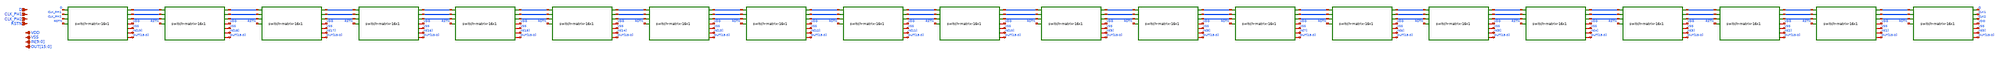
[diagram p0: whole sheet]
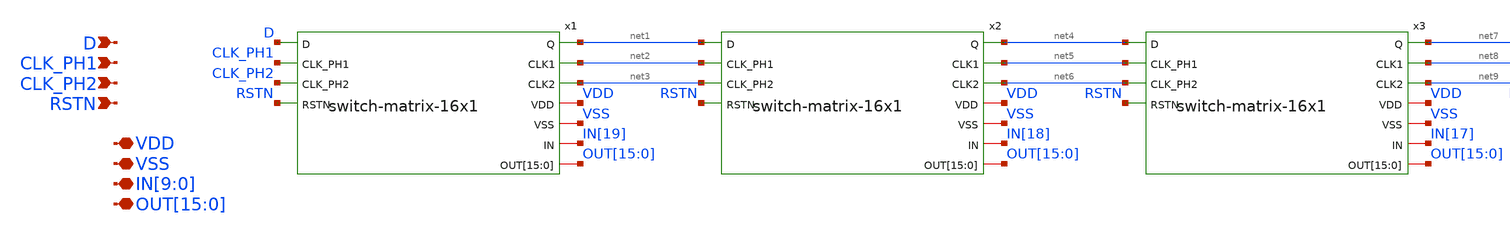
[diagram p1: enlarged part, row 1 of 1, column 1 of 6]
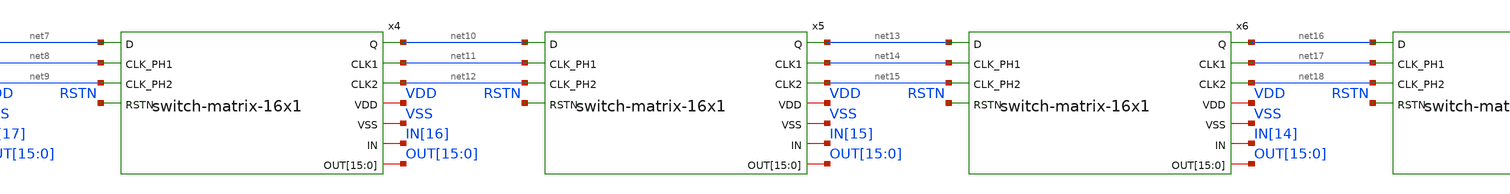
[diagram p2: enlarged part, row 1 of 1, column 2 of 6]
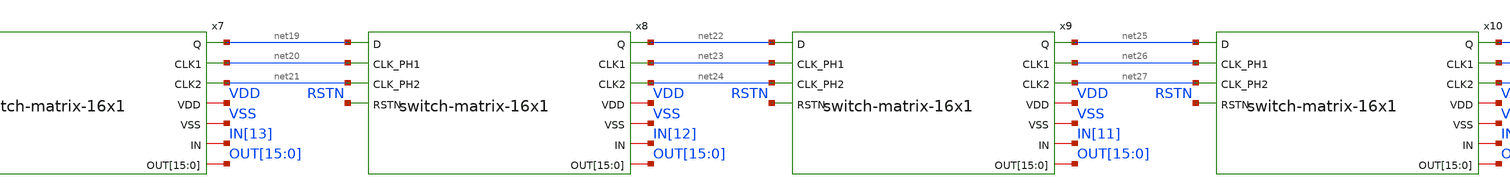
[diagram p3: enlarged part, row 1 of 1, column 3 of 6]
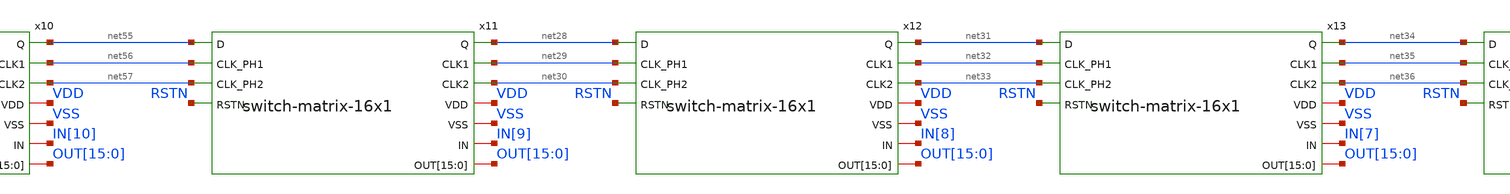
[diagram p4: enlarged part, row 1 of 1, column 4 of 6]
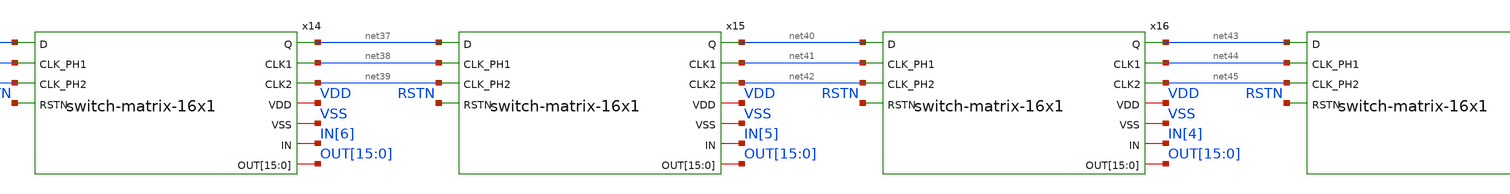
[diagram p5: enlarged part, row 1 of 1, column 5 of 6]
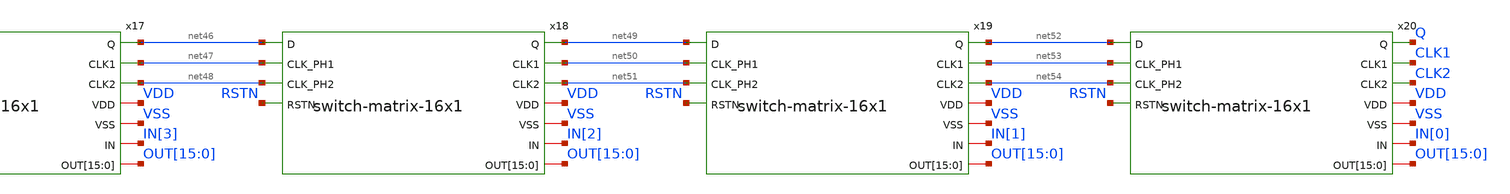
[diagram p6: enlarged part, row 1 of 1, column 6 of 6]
** sch_path: designs/libs/core_switch-matrix/switch-matrix-16x20/untitled-1.sch
**.subckt untitled-1 D CLK_PH1 CLK_PH2 RSTN VDD VSS
*+ IN[9],IN[8],IN[7],IN[6],IN[5],IN[4],IN[3],IN[2],IN[1],IN[0]
*+ OUT[15],OUT[14],OUT[13],OUT[12],OUT[11],OUT[10],OUT[9],OUT[8],OUT[7],OUT[6],OUT[5],OUT[4],OUT[3],OUT[2],OUT[1],OUT[0]
*.ipin D
*.ipin CLK_PH1
*.ipin CLK_PH2
*.ipin RSTN
*.iopin VDD
*.iopin VSS
*.iopin IN[9],IN[8],IN[7],IN[6],IN[5],IN[4],IN[3],IN[2],IN[1],IN[0]
*.iopin
*+ OUT[15],OUT[14],OUT[13],OUT[12],OUT[11],OUT[10],OUT[9],OUT[8],OUT[7],OUT[6],OUT[5],OUT[4],OUT[3],OUT[2],OUT[1],OUT[0]
x1 net1 net2 net3 VDD VSS IN[19] OUT[15] OUT[14] OUT[13] OUT[12] OUT[11] OUT[10] OUT[9] OUT[8]
+ OUT[7] OUT[6] OUT[5] OUT[4] OUT[3] OUT[2] OUT[1] OUT[0] D CLK_PH1 CLK_PH2 RSTN switch-matrix-16x1
x2 net4 net5 net6 VDD VSS IN[18] OUT[15] OUT[14] OUT[13] OUT[12] OUT[11] OUT[10] OUT[9] OUT[8]
+ OUT[7] OUT[6] OUT[5] OUT[4] OUT[3] OUT[2] OUT[1] OUT[0] net1 net2 net3 RSTN switch-matrix-16x1
x3 net7 net8 net9 VDD VSS IN[17] OUT[15] OUT[14] OUT[13] OUT[12] OUT[11] OUT[10] OUT[9] OUT[8]
+ OUT[7] OUT[6] OUT[5] OUT[4] OUT[3] OUT[2] OUT[1] OUT[0] net4 net5 net6 RSTN switch-matrix-16x1
x4 net10 net11 net12 VDD VSS IN[16] OUT[15] OUT[14] OUT[13] OUT[12] OUT[11] OUT[10] OUT[9] OUT[8]
+ OUT[7] OUT[6] OUT[5] OUT[4] OUT[3] OUT[2] OUT[1] OUT[0] net7 net8 net9 RSTN switch-matrix-16x1
x5 net13 net14 net15 VDD VSS IN[15] OUT[15] OUT[14] OUT[13] OUT[12] OUT[11] OUT[10] OUT[9] OUT[8]
+ OUT[7] OUT[6] OUT[5] OUT[4] OUT[3] OUT[2] OUT[1] OUT[0] net10 net11 net12 RSTN switch-matrix-16x1
x6 net16 net17 net18 VDD VSS IN[14] OUT[15] OUT[14] OUT[13] OUT[12] OUT[11] OUT[10] OUT[9] OUT[8]
+ OUT[7] OUT[6] OUT[5] OUT[4] OUT[3] OUT[2] OUT[1] OUT[0] net13 net14 net15 RSTN switch-matrix-16x1
x7 net19 net20 net21 VDD VSS IN[13] OUT[15] OUT[14] OUT[13] OUT[12] OUT[11] OUT[10] OUT[9] OUT[8]
+ OUT[7] OUT[6] OUT[5] OUT[4] OUT[3] OUT[2] OUT[1] OUT[0] net16 net17 net18 RSTN switch-matrix-16x1
x8 net22 net23 net24 VDD VSS IN[12] OUT[15] OUT[14] OUT[13] OUT[12] OUT[11] OUT[10] OUT[9] OUT[8]
+ OUT[7] OUT[6] OUT[5] OUT[4] OUT[3] OUT[2] OUT[1] OUT[0] net19 net20 net21 RSTN switch-matrix-16x1
x9 net25 net26 net27 VDD VSS IN[11] OUT[15] OUT[14] OUT[13] OUT[12] OUT[11] OUT[10] OUT[9] OUT[8]
+ OUT[7] OUT[6] OUT[5] OUT[4] OUT[3] OUT[2] OUT[1] OUT[0] net22 net23 net24 RSTN switch-matrix-16x1
x10 net55 net56 net57 VDD VSS IN[10] OUT[15] OUT[14] OUT[13] OUT[12] OUT[11] OUT[10] OUT[9] OUT[8]
+ OUT[7] OUT[6] OUT[5] OUT[4] OUT[3] OUT[2] OUT[1] OUT[0] net25 net26 net27 RSTN switch-matrix-16x1
x11 net28 net29 net30 VDD VSS IN[9] OUT[15] OUT[14] OUT[13] OUT[12] OUT[11] OUT[10] OUT[9] OUT[8]
+ OUT[7] OUT[6] OUT[5] OUT[4] OUT[3] OUT[2] OUT[1] OUT[0] net55 net56 net57 RSTN switch-matrix-16x1
x12 net31 net32 net33 VDD VSS IN[8] OUT[15] OUT[14] OUT[13] OUT[12] OUT[11] OUT[10] OUT[9] OUT[8]
+ OUT[7] OUT[6] OUT[5] OUT[4] OUT[3] OUT[2] OUT[1] OUT[0] net28 net29 net30 RSTN switch-matrix-16x1
x13 net34 net35 net36 VDD VSS IN[7] OUT[15] OUT[14] OUT[13] OUT[12] OUT[11] OUT[10] OUT[9] OUT[8]
+ OUT[7] OUT[6] OUT[5] OUT[4] OUT[3] OUT[2] OUT[1] OUT[0] net31 net32 net33 RSTN switch-matrix-16x1
x14 net37 net38 net39 VDD VSS IN[6] OUT[15] OUT[14] OUT[13] OUT[12] OUT[11] OUT[10] OUT[9] OUT[8]
+ OUT[7] OUT[6] OUT[5] OUT[4] OUT[3] OUT[2] OUT[1] OUT[0] net34 net35 net36 RSTN switch-matrix-16x1
x15 net40 net41 net42 VDD VSS IN[5] OUT[15] OUT[14] OUT[13] OUT[12] OUT[11] OUT[10] OUT[9] OUT[8]
+ OUT[7] OUT[6] OUT[5] OUT[4] OUT[3] OUT[2] OUT[1] OUT[0] net37 net38 net39 RSTN switch-matrix-16x1
x16 net43 net44 net45 VDD VSS IN[4] OUT[15] OUT[14] OUT[13] OUT[12] OUT[11] OUT[10] OUT[9] OUT[8]
+ OUT[7] OUT[6] OUT[5] OUT[4] OUT[3] OUT[2] OUT[1] OUT[0] net40 net41 net42 RSTN switch-matrix-16x1
x17 net46 net47 net48 VDD VSS IN[3] OUT[15] OUT[14] OUT[13] OUT[12] OUT[11] OUT[10] OUT[9] OUT[8]
+ OUT[7] OUT[6] OUT[5] OUT[4] OUT[3] OUT[2] OUT[1] OUT[0] net43 net44 net45 RSTN switch-matrix-16x1
x18 net49 net50 net51 VDD VSS IN[2] OUT[15] OUT[14] OUT[13] OUT[12] OUT[11] OUT[10] OUT[9] OUT[8]
+ OUT[7] OUT[6] OUT[5] OUT[4] OUT[3] OUT[2] OUT[1] OUT[0] net46 net47 net48 RSTN switch-matrix-16x1
x19 net52 net53 net54 VDD VSS IN[1] OUT[15] OUT[14] OUT[13] OUT[12] OUT[11] OUT[10] OUT[9] OUT[8]
+ OUT[7] OUT[6] OUT[5] OUT[4] OUT[3] OUT[2] OUT[1] OUT[0] net49 net50 net51 RSTN switch-matrix-16x1
x20 Q CLK1 CLK2 VDD VSS IN[0] OUT[15] OUT[14] OUT[13] OUT[12] OUT[11] OUT[10] OUT[9] OUT[8] OUT[7]
+ OUT[6] OUT[5] OUT[4] OUT[3] OUT[2] OUT[1] OUT[0] net52 net53 net54 RSTN switch-matrix-16x1
**.ends
.end
